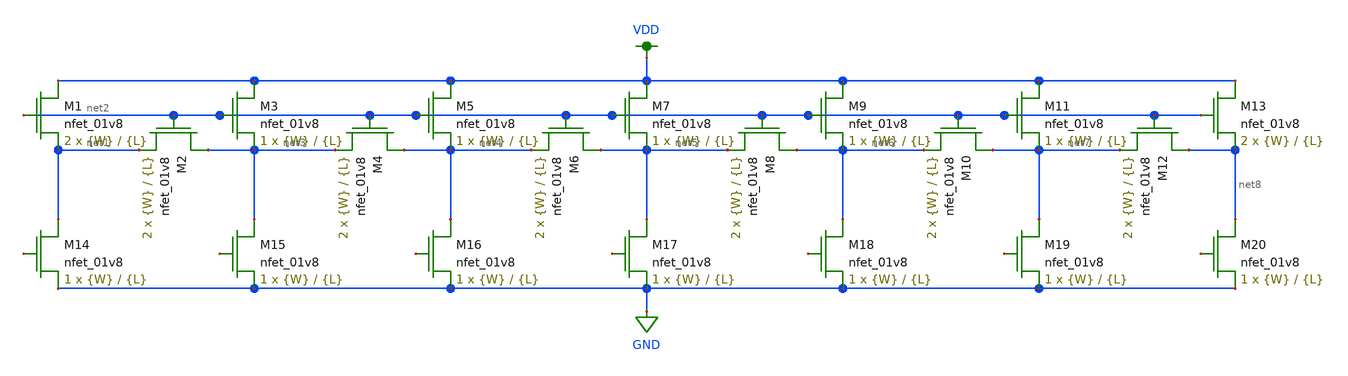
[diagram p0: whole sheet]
** sch_path: schematics/please_work_dac.sch
**.subckt please_work_dac
XM1 VDD net2 net1 GND sky130_fd_pr__nfet_01v8 L={L} W={W} nf=1 ad='int((nf+1)/2) * W/nf * 0.29' as='int((nf+2)/2) * W/nf * 0.29'
+ pd='2*int((nf+1)/2) * (W/nf + 0.29)' ps='2*int((nf+2)/2) * (W/nf + 0.29)' nrd='0.29 / W' nrs='0.29 / W'
+ sa=0 sb=0 sd=0 mult=2 m=2
XM2 net3 net2 net1 GND sky130_fd_pr__nfet_01v8 L={L} W={W} nf=1 ad='int((nf+1)/2) * W/nf * 0.29' as='int((nf+2)/2) * W/nf * 0.29'
+ pd='2*int((nf+1)/2) * (W/nf + 0.29)' ps='2*int((nf+2)/2) * (W/nf + 0.29)' nrd='0.29 / W' nrs='0.29 / W'
+ sa=0 sb=0 sd=0 mult=2 m=2
XM3 VDD net2 net3 GND sky130_fd_pr__nfet_01v8 L={L} W={W} nf=1 ad='int((nf+1)/2) * W/nf * 0.29' as='int((nf+2)/2) * W/nf * 0.29'
+ pd='2*int((nf+1)/2) * (W/nf + 0.29)' ps='2*int((nf+2)/2) * (W/nf + 0.29)' nrd='0.29 / W' nrs='0.29 / W'
+ sa=0 sb=0 sd=0 mult=1 m=1
XM4 net4 net2 net3 GND sky130_fd_pr__nfet_01v8 L={L} W={W} nf=1 ad='int((nf+1)/2) * W/nf * 0.29' as='int((nf+2)/2) * W/nf * 0.29'
+ pd='2*int((nf+1)/2) * (W/nf + 0.29)' ps='2*int((nf+2)/2) * (W/nf + 0.29)' nrd='0.29 / W' nrs='0.29 / W'
+ sa=0 sb=0 sd=0 mult=2 m=2
XM5 VDD net2 net4 GND sky130_fd_pr__nfet_01v8 L={L} W={W} nf=1 ad='int((nf+1)/2) * W/nf * 0.29' as='int((nf+2)/2) * W/nf * 0.29'
+ pd='2*int((nf+1)/2) * (W/nf + 0.29)' ps='2*int((nf+2)/2) * (W/nf + 0.29)' nrd='0.29 / W' nrs='0.29 / W'
+ sa=0 sb=0 sd=0 mult=1 m=1
XM6 net5 net2 net4 GND sky130_fd_pr__nfet_01v8 L={L} W={W} nf=1 ad='int((nf+1)/2) * W/nf * 0.29' as='int((nf+2)/2) * W/nf * 0.29'
+ pd='2*int((nf+1)/2) * (W/nf + 0.29)' ps='2*int((nf+2)/2) * (W/nf + 0.29)' nrd='0.29 / W' nrs='0.29 / W'
+ sa=0 sb=0 sd=0 mult=2 m=2
XM7 VDD net2 net5 GND sky130_fd_pr__nfet_01v8 L={L} W={W} nf=1 ad='int((nf+1)/2) * W/nf * 0.29' as='int((nf+2)/2) * W/nf * 0.29'
+ pd='2*int((nf+1)/2) * (W/nf + 0.29)' ps='2*int((nf+2)/2) * (W/nf + 0.29)' nrd='0.29 / W' nrs='0.29 / W'
+ sa=0 sb=0 sd=0 mult=1 m=1
XM8 net6 net2 net5 GND sky130_fd_pr__nfet_01v8 L={L} W={W} nf=1 ad='int((nf+1)/2) * W/nf * 0.29' as='int((nf+2)/2) * W/nf * 0.29'
+ pd='2*int((nf+1)/2) * (W/nf + 0.29)' ps='2*int((nf+2)/2) * (W/nf + 0.29)' nrd='0.29 / W' nrs='0.29 / W'
+ sa=0 sb=0 sd=0 mult=2 m=2
XM9 VDD net2 net6 GND sky130_fd_pr__nfet_01v8 L={L} W={W} nf=1 ad='int((nf+1)/2) * W/nf * 0.29' as='int((nf+2)/2) * W/nf * 0.29'
+ pd='2*int((nf+1)/2) * (W/nf + 0.29)' ps='2*int((nf+2)/2) * (W/nf + 0.29)' nrd='0.29 / W' nrs='0.29 / W'
+ sa=0 sb=0 sd=0 mult=1 m=1
XM10 net7 net2 net6 GND sky130_fd_pr__nfet_01v8 L={L} W={W} nf=1 ad='int((nf+1)/2) * W/nf * 0.29' as='int((nf+2)/2) * W/nf * 0.29'
+ pd='2*int((nf+1)/2) * (W/nf + 0.29)' ps='2*int((nf+2)/2) * (W/nf + 0.29)' nrd='0.29 / W' nrs='0.29 / W'
+ sa=0 sb=0 sd=0 mult=2 m=2
XM11 VDD net2 net7 GND sky130_fd_pr__nfet_01v8 L={L} W={W} nf=1 ad='int((nf+1)/2) * W/nf * 0.29' as='int((nf+2)/2) * W/nf * 0.29'
+ pd='2*int((nf+1)/2) * (W/nf + 0.29)' ps='2*int((nf+2)/2) * (W/nf + 0.29)' nrd='0.29 / W' nrs='0.29 / W'
+ sa=0 sb=0 sd=0 mult=1 m=1
XM12 net8 net2 net7 GND sky130_fd_pr__nfet_01v8 L={L} W={W} nf=1 ad='int((nf+1)/2) * W/nf * 0.29' as='int((nf+2)/2) * W/nf * 0.29'
+ pd='2*int((nf+1)/2) * (W/nf + 0.29)' ps='2*int((nf+2)/2) * (W/nf + 0.29)' nrd='0.29 / W' nrs='0.29 / W'
+ sa=0 sb=0 sd=0 mult=2 m=2
XM13 VDD net2 net8 GND sky130_fd_pr__nfet_01v8 L={L} W={W} nf=1 ad='int((nf+1)/2) * W/nf * 0.29' as='int((nf+2)/2) * W/nf * 0.29'
+ pd='2*int((nf+1)/2) * (W/nf + 0.29)' ps='2*int((nf+2)/2) * (W/nf + 0.29)' nrd='0.29 / W' nrs='0.29 / W'
+ sa=0 sb=0 sd=0 mult=2 m=2
XM14 net1 net9 GND GND sky130_fd_pr__nfet_01v8 L={L} W={W} nf=1 ad='int((nf+1)/2) * W/nf * 0.29' as='int((nf+2)/2) * W/nf * 0.29'
+ pd='2*int((nf+1)/2) * (W/nf + 0.29)' ps='2*int((nf+2)/2) * (W/nf + 0.29)' nrd='0.29 / W' nrs='0.29 / W'
+ sa=0 sb=0 sd=0 mult=1 m=1
XM15 net3 net10 GND GND sky130_fd_pr__nfet_01v8 L={L} W={W} nf=1 ad='int((nf+1)/2) * W/nf * 0.29' as='int((nf+2)/2) * W/nf * 0.29'
+ pd='2*int((nf+1)/2) * (W/nf + 0.29)' ps='2*int((nf+2)/2) * (W/nf + 0.29)' nrd='0.29 / W' nrs='0.29 / W'
+ sa=0 sb=0 sd=0 mult=1 m=1
XM16 net4 net11 GND GND sky130_fd_pr__nfet_01v8 L={L} W={W} nf=1 ad='int((nf+1)/2) * W/nf * 0.29' as='int((nf+2)/2) * W/nf * 0.29'
+ pd='2*int((nf+1)/2) * (W/nf + 0.29)' ps='2*int((nf+2)/2) * (W/nf + 0.29)' nrd='0.29 / W' nrs='0.29 / W'
+ sa=0 sb=0 sd=0 mult=1 m=1
XM17 net5 net12 GND GND sky130_fd_pr__nfet_01v8 L={L} W={W} nf=1 ad='int((nf+1)/2) * W/nf * 0.29' as='int((nf+2)/2) * W/nf * 0.29'
+ pd='2*int((nf+1)/2) * (W/nf + 0.29)' ps='2*int((nf+2)/2) * (W/nf + 0.29)' nrd='0.29 / W' nrs='0.29 / W'
+ sa=0 sb=0 sd=0 mult=1 m=1
XM18 net6 net13 GND GND sky130_fd_pr__nfet_01v8 L={L} W={W} nf=1 ad='int((nf+1)/2) * W/nf * 0.29' as='int((nf+2)/2) * W/nf * 0.29'
+ pd='2*int((nf+1)/2) * (W/nf + 0.29)' ps='2*int((nf+2)/2) * (W/nf + 0.29)' nrd='0.29 / W' nrs='0.29 / W'
+ sa=0 sb=0 sd=0 mult=1 m=1
XM19 net7 net14 GND GND sky130_fd_pr__nfet_01v8 L={L} W={W} nf=1 ad='int((nf+1)/2) * W/nf * 0.29' as='int((nf+2)/2) * W/nf * 0.29'
+ pd='2*int((nf+1)/2) * (W/nf + 0.29)' ps='2*int((nf+2)/2) * (W/nf + 0.29)' nrd='0.29 / W' nrs='0.29 / W'
+ sa=0 sb=0 sd=0 mult=1 m=1
XM20 net8 net15 GND GND sky130_fd_pr__nfet_01v8 L={L} W={W} nf=1 ad='int((nf+1)/2) * W/nf * 0.29' as='int((nf+2)/2) * W/nf * 0.29'
+ pd='2*int((nf+1)/2) * (W/nf + 0.29)' ps='2*int((nf+2)/2) * (W/nf + 0.29)' nrd='0.29 / W' nrs='0.29 / W'
+ sa=0 sb=0 sd=0 mult=1 m=1
**.ends
.GLOBAL GND
.GLOBAL VDD
.end
